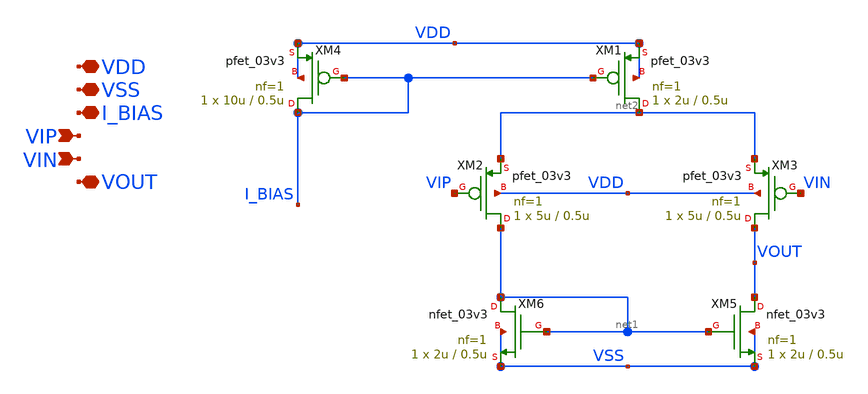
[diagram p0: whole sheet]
** sch_path: designs/libs/core_analog/p-ota/p-ota-5t.sch
**.subckt p-ota-5t VDD VSS I_BIAS VIP VIN VOUT
*.iopin VDD
*.iopin VSS
*.iopin I_BIAS
*.ipin VIP
*.ipin VIN
*.iopin VOUT
XM1 net2 I_BIAS VDD VDD pfet_03v3 L=0.5u W=2u nf=1 ad='int((nf+1)/2) * W/nf * 0.18u' as='int((nf+2)/2) * W/nf * 0.18u'
+ pd='2*int((nf+1)/2) * (W/nf + 0.18u)' ps='2*int((nf+2)/2) * (W/nf + 0.18u)' nrd='0.18u / W' nrs='0.18u / W'
+ sa=0 sb=0 sd=0 m=1
XM2 net1 VIP net2 VDD pfet_03v3 L=0.5u W=5u nf=1 ad='int((nf+1)/2) * W/nf * 0.18u' as='int((nf+2)/2) * W/nf * 0.18u'
+ pd='2*int((nf+1)/2) * (W/nf + 0.18u)' ps='2*int((nf+2)/2) * (W/nf + 0.18u)' nrd='0.18u / W' nrs='0.18u / W'
+ sa=0 sb=0 sd=0 m=1
XM3 VOUT VIN net2 VDD pfet_03v3 L=0.5u W=5u nf=1 ad='int((nf+1)/2) * W/nf * 0.18u' as='int((nf+2)/2) * W/nf * 0.18u'
+ pd='2*int((nf+1)/2) * (W/nf + 0.18u)' ps='2*int((nf+2)/2) * (W/nf + 0.18u)' nrd='0.18u / W' nrs='0.18u / W'
+ sa=0 sb=0 sd=0 m=1
XM4 I_BIAS I_BIAS VDD VDD pfet_03v3 L=0.5u W=10u nf=1 ad='int((nf+1)/2) * W/nf * 0.18u' as='int((nf+2)/2) * W/nf * 0.18u'
+ pd='2*int((nf+1)/2) * (W/nf + 0.18u)' ps='2*int((nf+2)/2) * (W/nf + 0.18u)' nrd='0.18u / W' nrs='0.18u / W'
+ sa=0 sb=0 sd=0 m=1
XM5 VOUT net1 VSS VSS nfet_03v3 L=0.5u W=2u nf=1 ad='int((nf+1)/2) * W/nf * 0.18u' as='int((nf+2)/2) * W/nf * 0.18u'
+ pd='2*int((nf+1)/2) * (W/nf + 0.18u)' ps='2*int((nf+2)/2) * (W/nf + 0.18u)' nrd='0.18u / W' nrs='0.18u / W'
+ sa=0 sb=0 sd=0 m=1
XM6 net1 net1 VSS VSS nfet_03v3 L=0.5u W=2u nf=1 ad='int((nf+1)/2) * W/nf * 0.18u' as='int((nf+2)/2) * W/nf * 0.18u'
+ pd='2*int((nf+1)/2) * (W/nf + 0.18u)' ps='2*int((nf+2)/2) * (W/nf + 0.18u)' nrd='0.18u / W' nrs='0.18u / W'
+ sa=0 sb=0 sd=0 m=1
**.ends
.end
